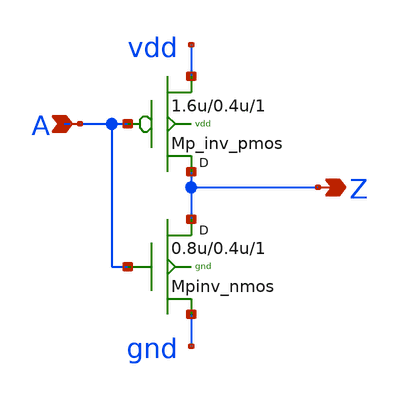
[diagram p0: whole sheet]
** sch_path: sram_2_64_scn4m_lcc/pinv_2.sch
**.subckt pinv_2 A Z
*.ipin A
*.opin Z
Mpinv_nmos Z A gnd gnd n w=0.8u l=0.4u m=1
Mp_inv_pmos Z A vdd vdd p w=1.6u l=0.4u m=1
**.ends
.end
